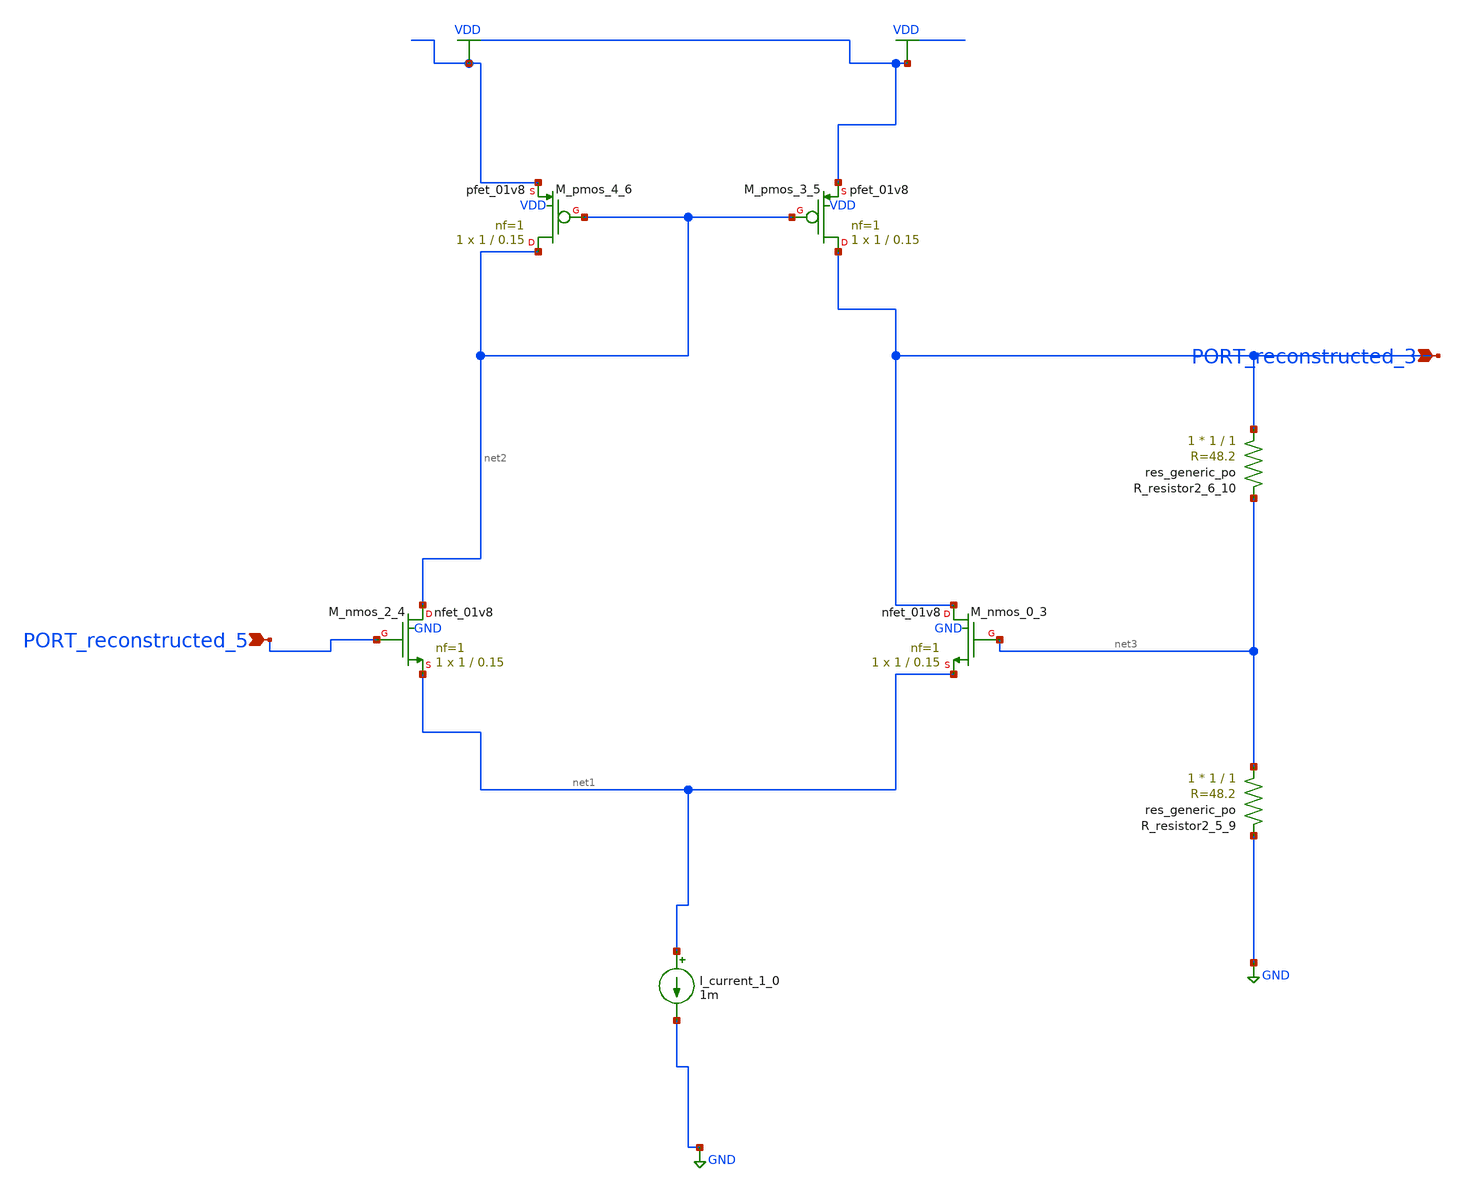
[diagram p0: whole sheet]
** sch_path: schematics/AMSNet/564.sch
**.subckt 564 PORT_reconstructed_5 PORT_reconstructed_3
*.ipin PORT_reconstructed_5
*.ipin PORT_reconstructed_3
I_current_1_0 net1 GND 1m
XM_nmos_0_3 PORT_reconstructed_3 net3 net1 GND sky130_fd_pr__nfet_01v8 L=0.15 W=1 nf=1 ad='int((1 + 1)/2) * 1 / 1 * 0.29'
+ as='int((1 + 2)/2) * 1 / 1 * 0.29' pd='2*int((1 + 1)/2) * (1 / 1 + 0.29)' ps='2*int((1 + 2)/2) * (1 / 1 + 0.29)'
+ nrd='0.29 / 1 ' nrs='0.29 / 1 ' sa=0 sb=0 sd=0 mult=1 m=1
XM_nmos_2_4 net2 PORT_reconstructed_5 net1 GND sky130_fd_pr__nfet_01v8 L=0.15 W=1 nf=1 ad='int((1 + 1)/2) * 1 / 1 * 0.29'
+ as='int((1 + 2)/2) * 1 / 1 * 0.29' pd='2*int((1 + 1)/2) * (1 / 1 + 0.29)' ps='2*int((1 + 2)/2) * (1 / 1 + 0.29)'
+ nrd='0.29 / 1 ' nrs='0.29 / 1 ' sa=0 sb=0 sd=0 mult=1 m=1
XM_pmos_3_5 PORT_reconstructed_3 net2 VDD VDD sky130_fd_pr__pfet_01v8 L=0.15 W=1 nf=1 ad='int((1 + 1)/2) * 1 / 1 * 0.29'
+ as='int((1 + 2)/2) * 1 / 1 * 0.29' pd='2*int((1 + 1)/2) * (1 / 1 + 0.29)' ps='2*int((1 + 2)/2) * (1 / 1 + 0.29)'
+ nrd='0.29 / 1 ' nrs='0.29 / 1 ' sa=0 sb=0 sd=0 mult=1 m=1
XM_pmos_4_6 net2 net2 VDD VDD sky130_fd_pr__pfet_01v8 L=0.15 W=1 nf=1 ad='int((1 + 1)/2) * 1 / 1 * 0.29'
+ as='int((1 + 2)/2) * 1 / 1 * 0.29' pd='2*int((1 + 1)/2) * (1 / 1 + 0.29)' ps='2*int((1 + 2)/2) * (1 / 1 + 0.29)'
+ nrd='0.29 / 1 ' nrs='0.29 / 1 ' sa=0 sb=0 sd=0 mult=1 m=1
XR_resistor2_5_9 net3 GND sky130_fd_pr__res_generic_po W=1 L=1 m=1
XR_resistor2_6_10 PORT_reconstructed_3 net3 sky130_fd_pr__res_generic_po W=1 L=1 m=1
**.ends
.GLOBAL GND
.GLOBAL VDD
.end
